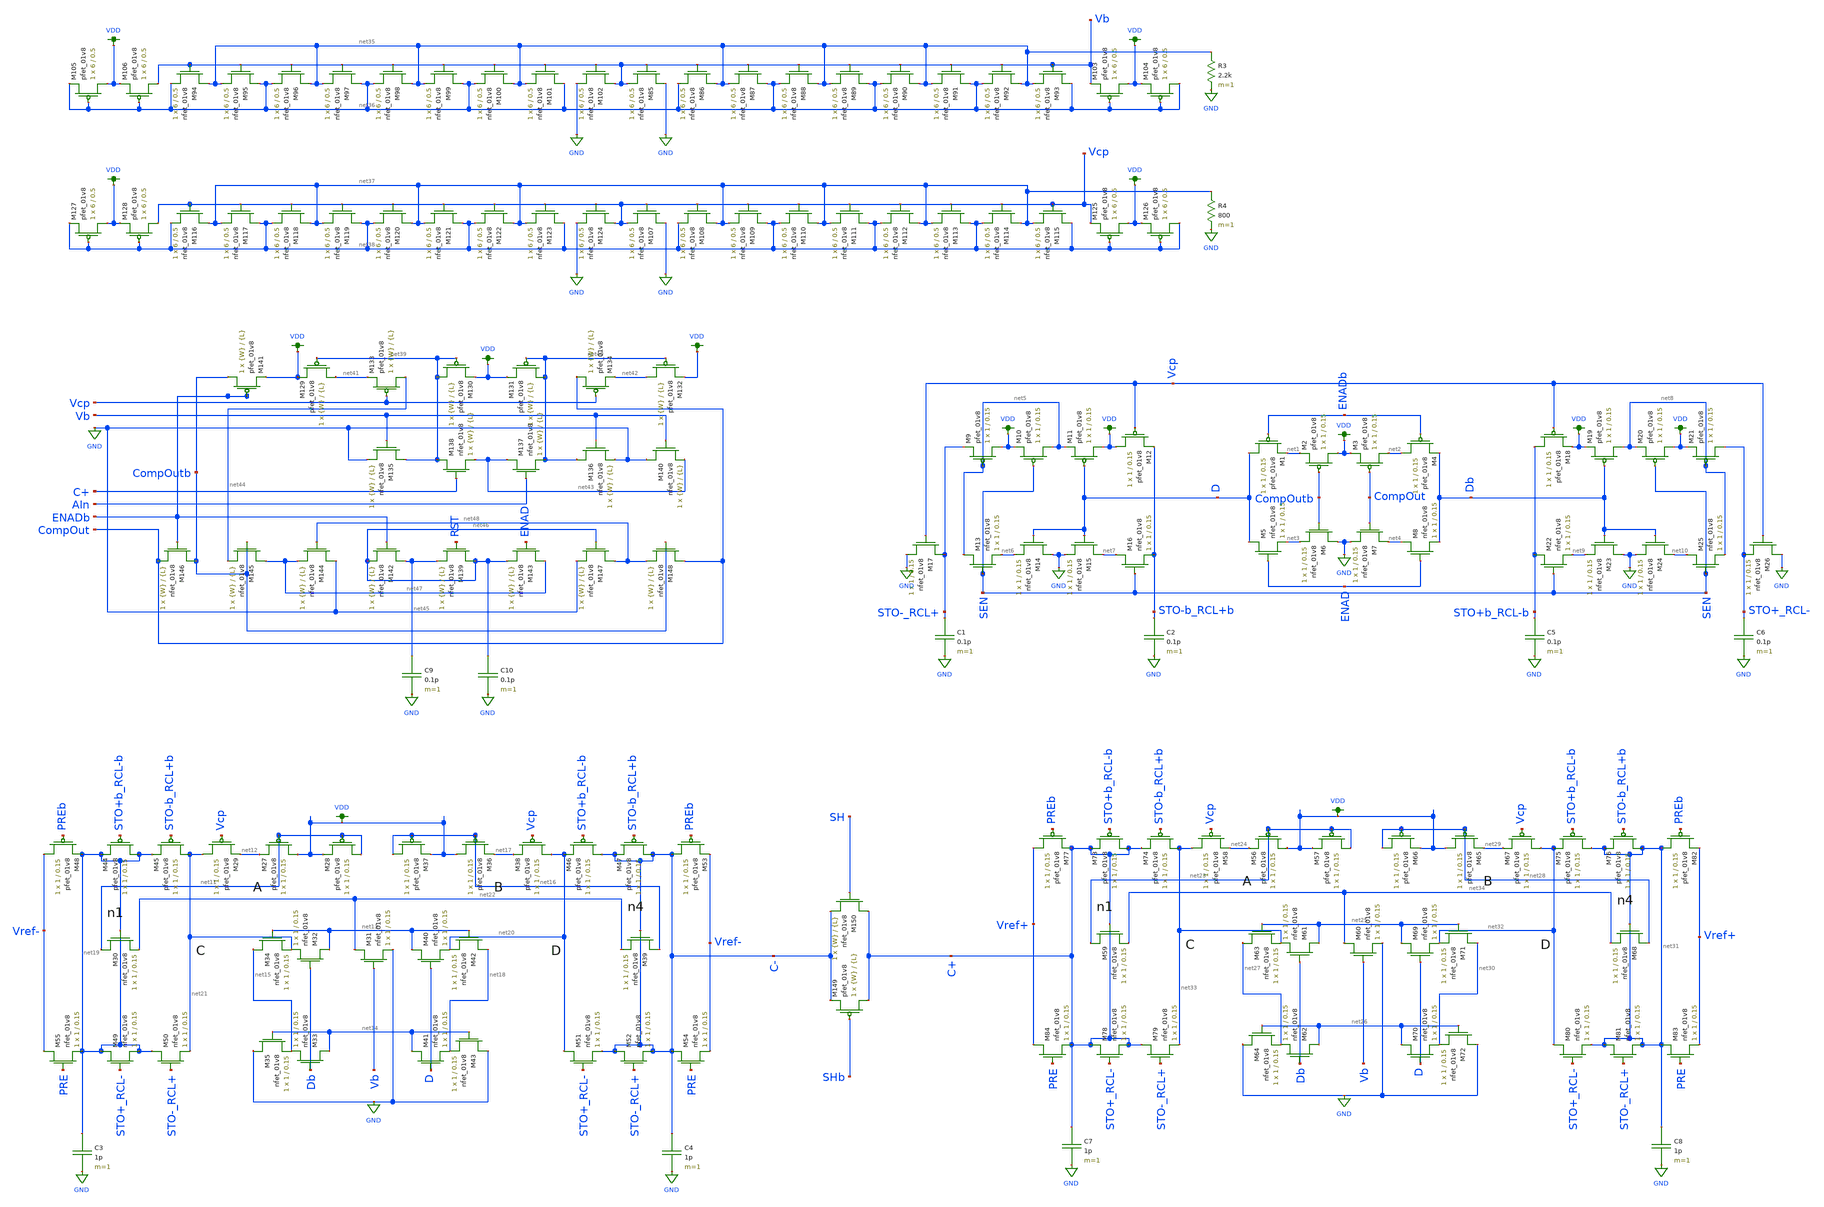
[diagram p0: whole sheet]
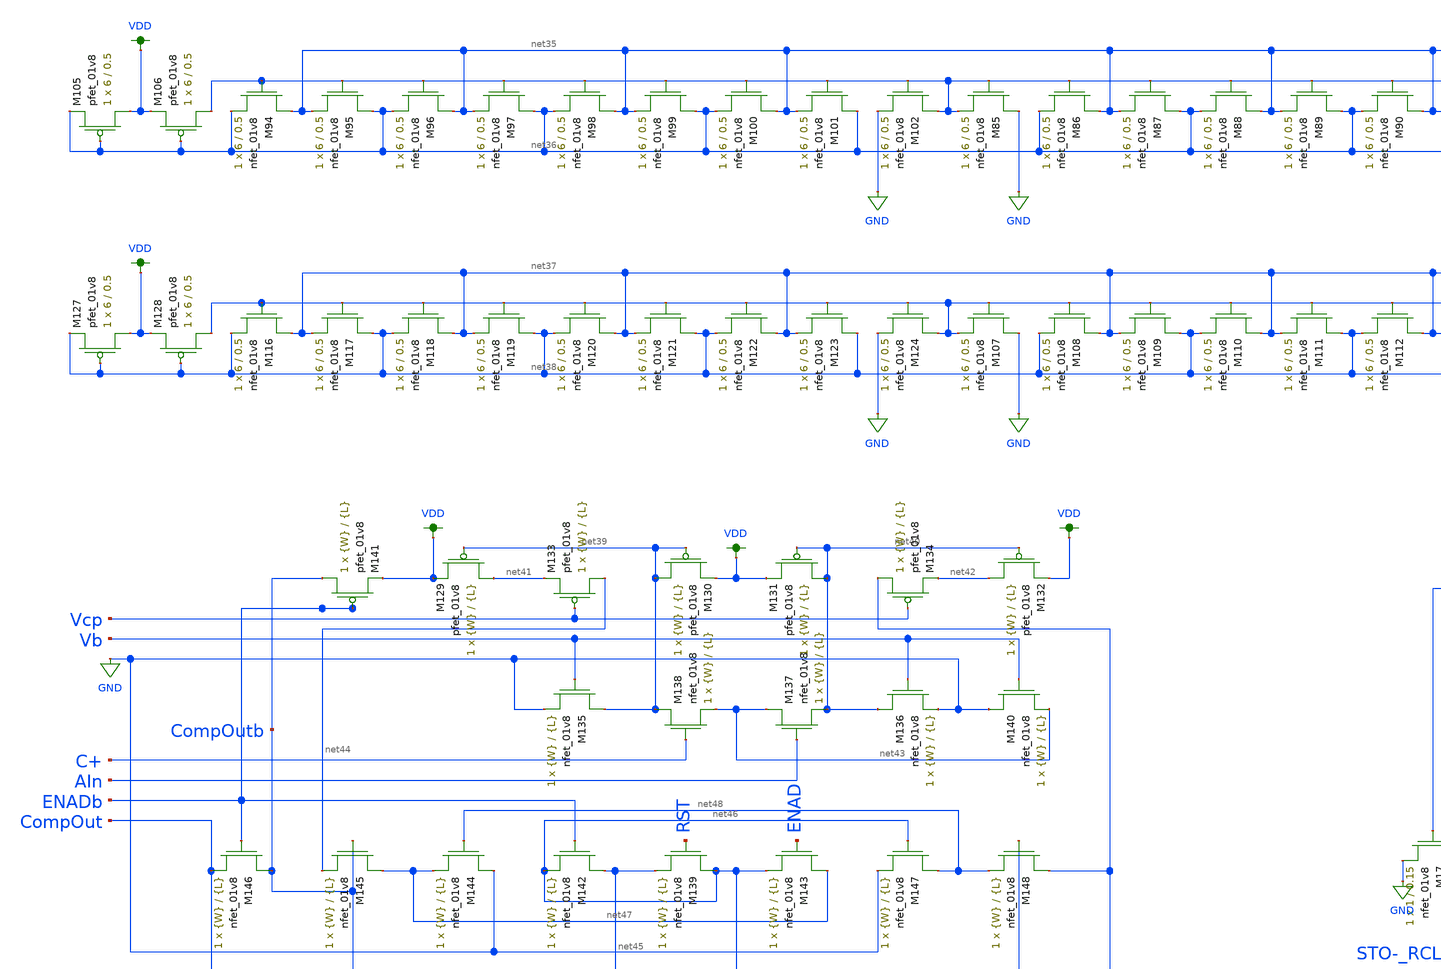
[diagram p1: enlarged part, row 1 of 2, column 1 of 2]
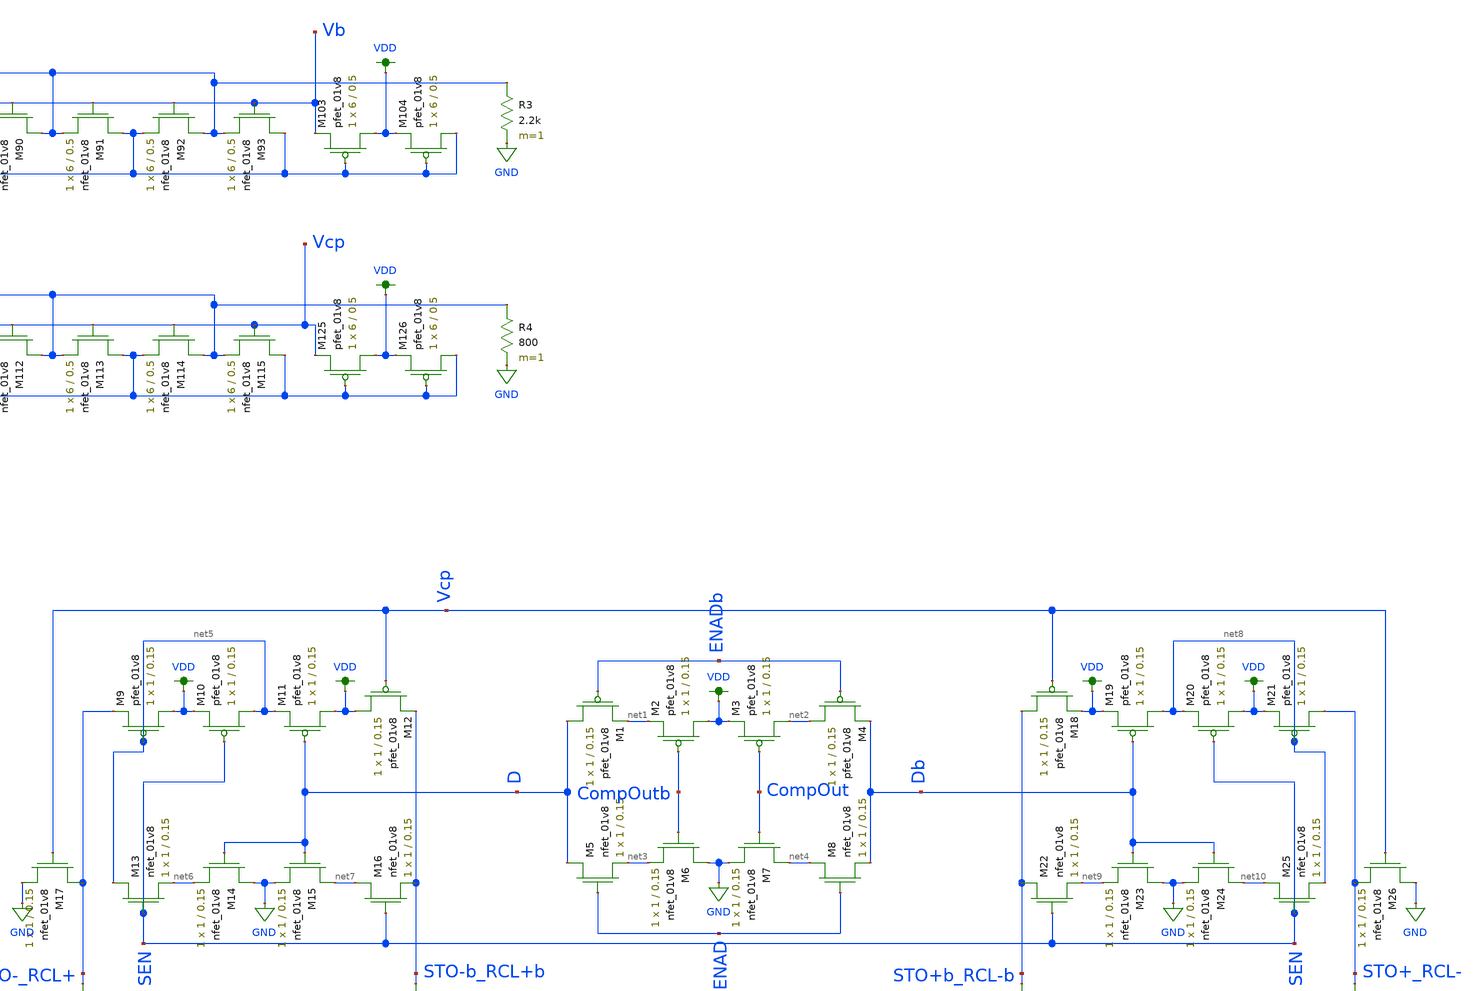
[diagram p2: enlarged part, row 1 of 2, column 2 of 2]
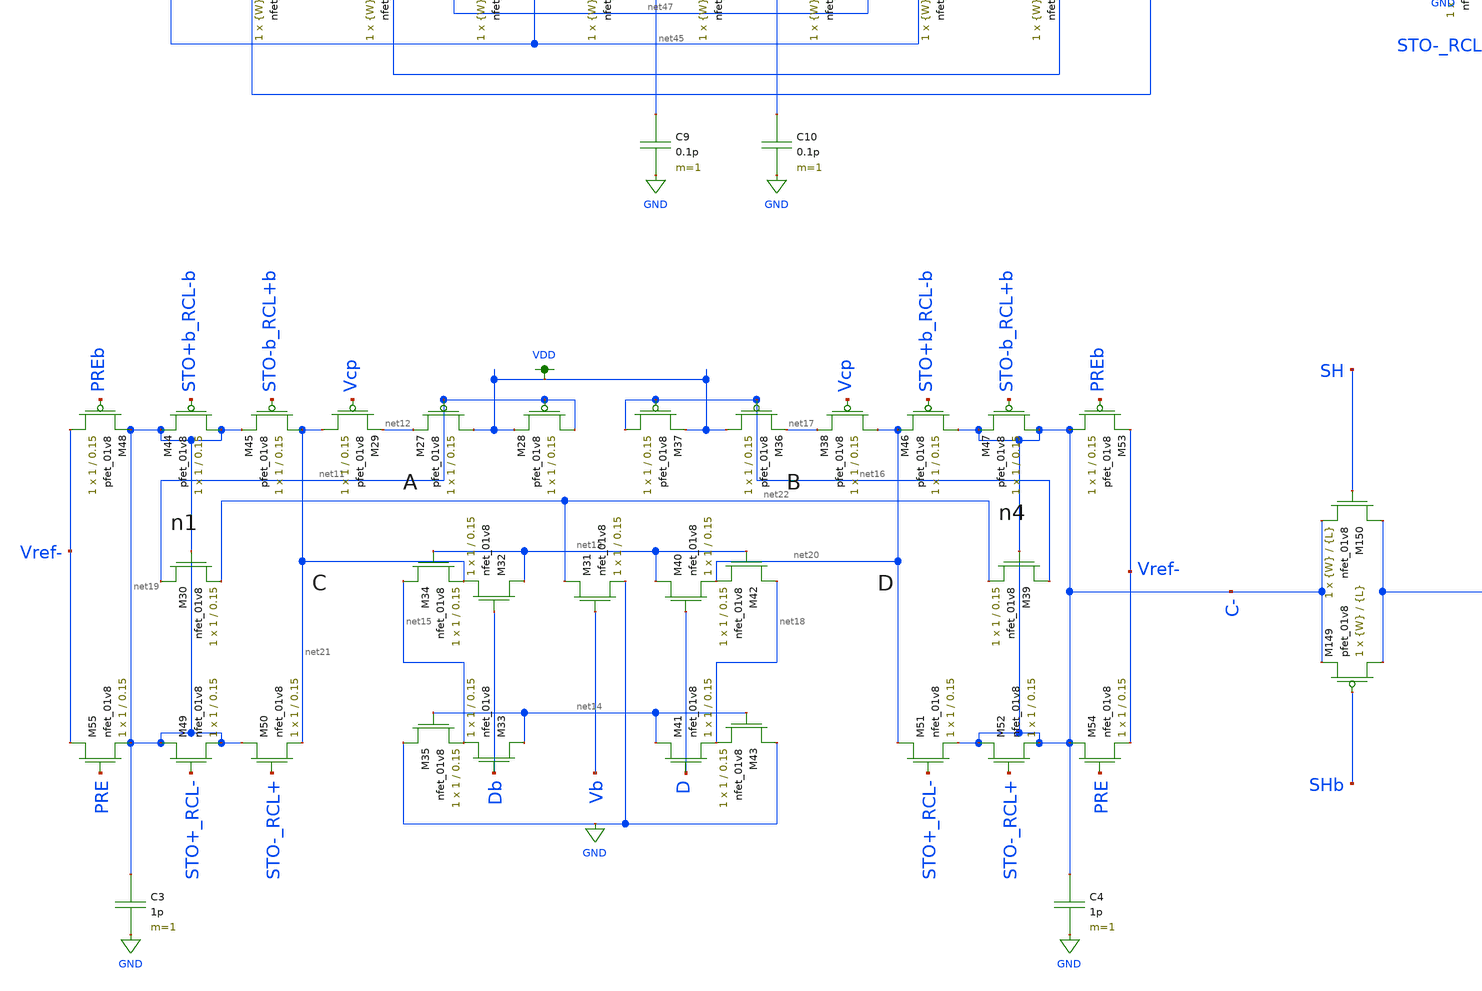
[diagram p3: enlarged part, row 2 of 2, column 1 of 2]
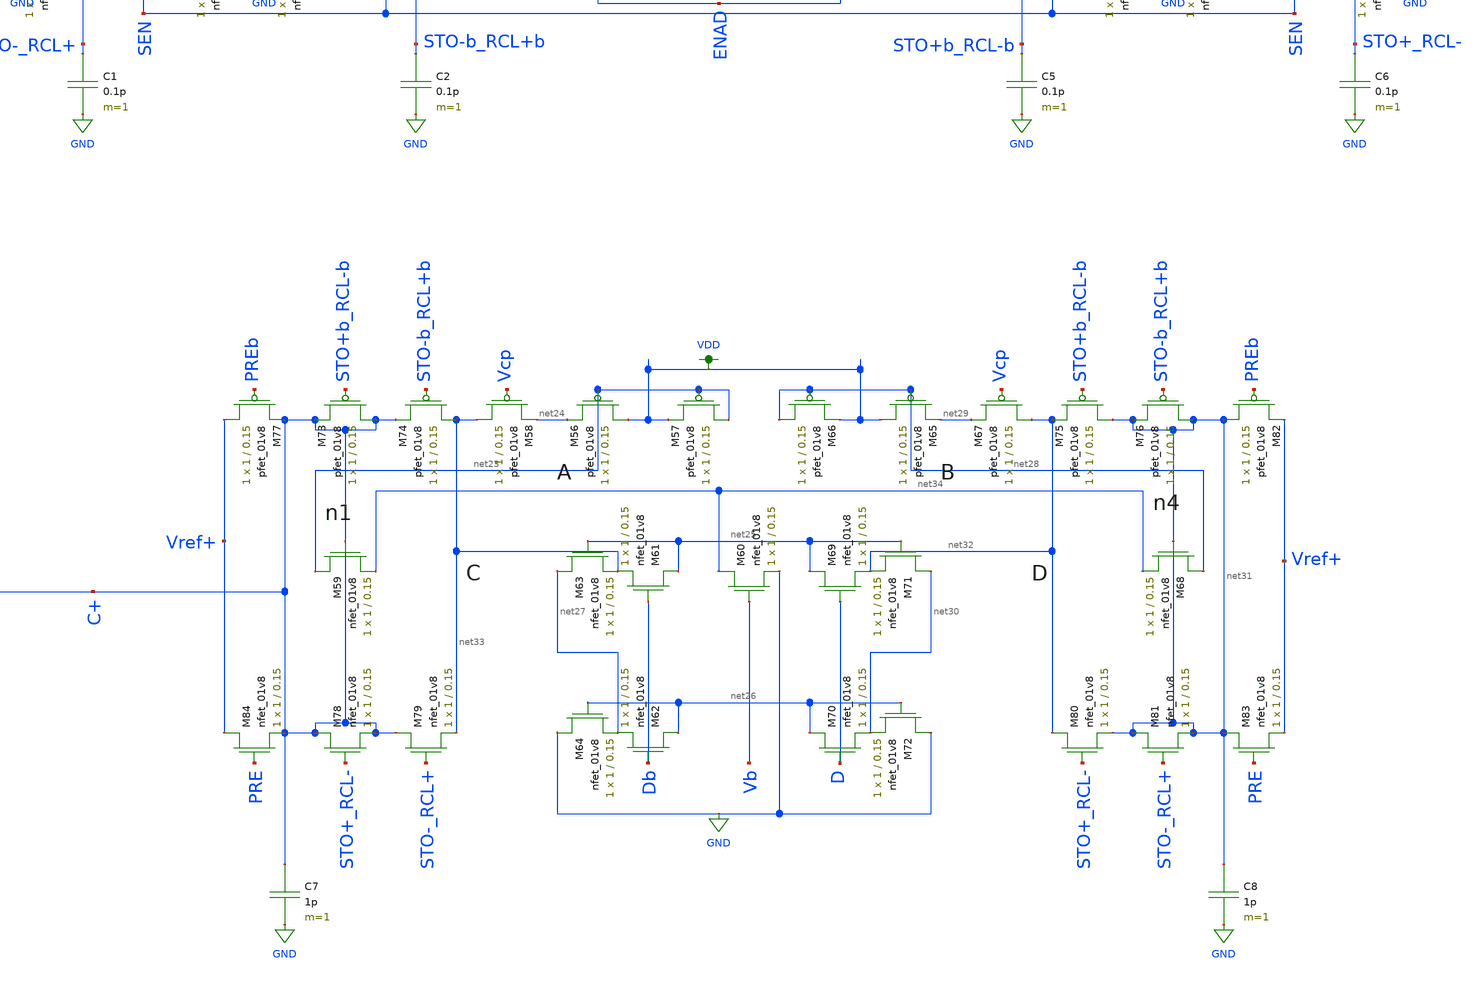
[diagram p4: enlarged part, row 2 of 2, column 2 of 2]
** sch_path: schematics/LDS/lds_schematics.sch
**.subckt lds_schematics
XM1 D ENADb net1 VDD sky130_fd_pr__pfet_01v8 L=0.15 W=1 nf=1 ad='int((nf+1)/2) * W/nf * 0.29' as='int((nf+2)/2) * W/nf * 0.29'
+ pd='2*int((nf+1)/2) * (W/nf + 0.29)' ps='2*int((nf+2)/2) * (W/nf + 0.29)' nrd='0.29 / W' nrs='0.29 / W'
+ sa=0 sb=0 sd=0 mult=1 m=1
XM2 VDD CompOutb net1 VDD sky130_fd_pr__pfet_01v8 L=0.15 W=1 nf=1 ad='int((nf+1)/2) * W/nf * 0.29' as='int((nf+2)/2) * W/nf * 0.29'
+ pd='2*int((nf+1)/2) * (W/nf + 0.29)' ps='2*int((nf+2)/2) * (W/nf + 0.29)' nrd='0.29 / W' nrs='0.29 / W'
+ sa=0 sb=0 sd=0 mult=1 m=1
XM3 net2 CompOut VDD VDD sky130_fd_pr__pfet_01v8 L=0.15 W=1 nf=1 ad='int((nf+1)/2) * W/nf * 0.29' as='int((nf+2)/2) * W/nf * 0.29'
+ pd='2*int((nf+1)/2) * (W/nf + 0.29)' ps='2*int((nf+2)/2) * (W/nf + 0.29)' nrd='0.29 / W' nrs='0.29 / W'
+ sa=0 sb=0 sd=0 mult=1 m=1
XM4 net2 ENADb Db VDD sky130_fd_pr__pfet_01v8 L=0.15 W=1 nf=1 ad='int((nf+1)/2) * W/nf * 0.29' as='int((nf+2)/2) * W/nf * 0.29'
+ pd='2*int((nf+1)/2) * (W/nf + 0.29)' ps='2*int((nf+2)/2) * (W/nf + 0.29)' nrd='0.29 / W' nrs='0.29 / W'
+ sa=0 sb=0 sd=0 mult=1 m=1
XM5 D ENAD net3 GND sky130_fd_pr__nfet_01v8 L=0.15 W=1 nf=1 ad='int((nf+1)/2) * W/nf * 0.29' as='int((nf+2)/2) * W/nf * 0.29'
+ pd='2*int((nf+1)/2) * (W/nf + 0.29)' ps='2*int((nf+2)/2) * (W/nf + 0.29)' nrd='0.29 / W' nrs='0.29 / W'
+ sa=0 sb=0 sd=0 mult=1 m=1
XM6 GND CompOutb net3 GND sky130_fd_pr__nfet_01v8 L=0.15 W=1 nf=1 ad='int((nf+1)/2) * W/nf * 0.29' as='int((nf+2)/2) * W/nf * 0.29'
+ pd='2*int((nf+1)/2) * (W/nf + 0.29)' ps='2*int((nf+2)/2) * (W/nf + 0.29)' nrd='0.29 / W' nrs='0.29 / W'
+ sa=0 sb=0 sd=0 mult=1 m=1
XM7 net4 CompOut GND GND sky130_fd_pr__nfet_01v8 L=0.15 W=1 nf=1 ad='int((nf+1)/2) * W/nf * 0.29' as='int((nf+2)/2) * W/nf * 0.29'
+ pd='2*int((nf+1)/2) * (W/nf + 0.29)' ps='2*int((nf+2)/2) * (W/nf + 0.29)' nrd='0.29 / W' nrs='0.29 / W'
+ sa=0 sb=0 sd=0 mult=1 m=1
XM8 net4 ENAD Db GND sky130_fd_pr__nfet_01v8 L=0.15 W=1 nf=1 ad='int((nf+1)/2) * W/nf * 0.29' as='int((nf+2)/2) * W/nf * 0.29'
+ pd='2*int((nf+1)/2) * (W/nf + 0.29)' ps='2*int((nf+2)/2) * (W/nf + 0.29)' nrd='0.29 / W' nrs='0.29 / W'
+ sa=0 sb=0 sd=0 mult=1 m=1
XM9 VDD net5 STO-_RCL+ VDD sky130_fd_pr__pfet_01v8 L=0.15 W=1 nf=1 ad='int((nf+1)/2) * W/nf * 0.29' as='int((nf+2)/2) * W/nf * 0.29'
+ pd='2*int((nf+1)/2) * (W/nf + 0.29)' ps='2*int((nf+2)/2) * (W/nf + 0.29)' nrd='0.29 / W' nrs='0.29 / W'
+ sa=0 sb=0 sd=0 mult=1 m=1
XM10 net5 SEN VDD VDD sky130_fd_pr__pfet_01v8 L=0.15 W=1 nf=1 ad='int((nf+1)/2) * W/nf * 0.29' as='int((nf+2)/2) * W/nf * 0.29'
+ pd='2*int((nf+1)/2) * (W/nf + 0.29)' ps='2*int((nf+2)/2) * (W/nf + 0.29)' nrd='0.29 / W' nrs='0.29 / W'
+ sa=0 sb=0 sd=0 mult=1 m=1
XM11 VDD D net5 VDD sky130_fd_pr__pfet_01v8 L=0.15 W=1 nf=1 ad='int((nf+1)/2) * W/nf * 0.29' as='int((nf+2)/2) * W/nf * 0.29'
+ pd='2*int((nf+1)/2) * (W/nf + 0.29)' ps='2*int((nf+2)/2) * (W/nf + 0.29)' nrd='0.29 / W' nrs='0.29 / W'
+ sa=0 sb=0 sd=0 mult=1 m=1
XM12 VDD Vcp STO-b_RCL+b VDD sky130_fd_pr__pfet_01v8 L=0.15 W=1 nf=1 ad='int((nf+1)/2) * W/nf * 0.29'
+ as='int((nf+2)/2) * W/nf * 0.29' pd='2*int((nf+1)/2) * (W/nf + 0.29)' ps='2*int((nf+2)/2) * (W/nf + 0.29)'
+ nrd='0.29 / W' nrs='0.29 / W' sa=0 sb=0 sd=0 mult=1 m=1
XM13 net5 SEN net6 GND sky130_fd_pr__nfet_01v8 L=0.15 W=1 nf=1 ad='int((nf+1)/2) * W/nf * 0.29' as='int((nf+2)/2) * W/nf * 0.29'
+ pd='2*int((nf+1)/2) * (W/nf + 0.29)' ps='2*int((nf+2)/2) * (W/nf + 0.29)' nrd='0.29 / W' nrs='0.29 / W'
+ sa=0 sb=0 sd=0 mult=1 m=1
XM14 GND D net6 GND sky130_fd_pr__nfet_01v8 L=0.15 W=1 nf=1 ad='int((nf+1)/2) * W/nf * 0.29' as='int((nf+2)/2) * W/nf * 0.29'
+ pd='2*int((nf+1)/2) * (W/nf + 0.29)' ps='2*int((nf+2)/2) * (W/nf + 0.29)' nrd='0.29 / W' nrs='0.29 / W'
+ sa=0 sb=0 sd=0 mult=1 m=1
XM15 net7 D GND GND sky130_fd_pr__nfet_01v8 L=0.15 W=1 nf=1 ad='int((nf+1)/2) * W/nf * 0.29' as='int((nf+2)/2) * W/nf * 0.29'
+ pd='2*int((nf+1)/2) * (W/nf + 0.29)' ps='2*int((nf+2)/2) * (W/nf + 0.29)' nrd='0.29 / W' nrs='0.29 / W'
+ sa=0 sb=0 sd=0 mult=1 m=1
XM16 net7 SEN STO-b_RCL+b GND sky130_fd_pr__nfet_01v8 L=0.15 W=1 nf=1 ad='int((nf+1)/2) * W/nf * 0.29'
+ as='int((nf+2)/2) * W/nf * 0.29' pd='2*int((nf+1)/2) * (W/nf + 0.29)' ps='2*int((nf+2)/2) * (W/nf + 0.29)'
+ nrd='0.29 / W' nrs='0.29 / W' sa=0 sb=0 sd=0 mult=1 m=1
XM17 STO-_RCL+ Vcp GND GND sky130_fd_pr__nfet_01v8 L=0.15 W=1 nf=1 ad='int((nf+1)/2) * W/nf * 0.29' as='int((nf+2)/2) * W/nf * 0.29'
+ pd='2*int((nf+1)/2) * (W/nf + 0.29)' ps='2*int((nf+2)/2) * (W/nf + 0.29)' nrd='0.29 / W' nrs='0.29 / W'
+ sa=0 sb=0 sd=0 mult=1 m=1
C1 STO-_RCL+ GND 0.1p m=1
C2 STO-b_RCL+b GND 0.1p m=1
XM18 STO+b_RCL-b Vcp VDD VDD sky130_fd_pr__pfet_01v8 L=0.15 W=1 nf=1 ad='int((nf+1)/2) * W/nf * 0.29'
+ as='int((nf+2)/2) * W/nf * 0.29' pd='2*int((nf+1)/2) * (W/nf + 0.29)' ps='2*int((nf+2)/2) * (W/nf + 0.29)'
+ nrd='0.29 / W' nrs='0.29 / W' sa=0 sb=0 sd=0 mult=1 m=1
XM19 net8 Db VDD VDD sky130_fd_pr__pfet_01v8 L=0.15 W=1 nf=1 ad='int((nf+1)/2) * W/nf * 0.29' as='int((nf+2)/2) * W/nf * 0.29'
+ pd='2*int((nf+1)/2) * (W/nf + 0.29)' ps='2*int((nf+2)/2) * (W/nf + 0.29)' nrd='0.29 / W' nrs='0.29 / W'
+ sa=0 sb=0 sd=0 mult=1 m=1
XM20 VDD SEN net8 VDD sky130_fd_pr__pfet_01v8 L=0.15 W=1 nf=1 ad='int((nf+1)/2) * W/nf * 0.29' as='int((nf+2)/2) * W/nf * 0.29'
+ pd='2*int((nf+1)/2) * (W/nf + 0.29)' ps='2*int((nf+2)/2) * (W/nf + 0.29)' nrd='0.29 / W' nrs='0.29 / W'
+ sa=0 sb=0 sd=0 mult=1 m=1
XM21 STO+_RCL- net8 VDD VDD sky130_fd_pr__pfet_01v8 L=0.15 W=1 nf=1 ad='int((nf+1)/2) * W/nf * 0.29'
+ as='int((nf+2)/2) * W/nf * 0.29' pd='2*int((nf+1)/2) * (W/nf + 0.29)' ps='2*int((nf+2)/2) * (W/nf + 0.29)'
+ nrd='0.29 / W' nrs='0.29 / W' sa=0 sb=0 sd=0 mult=1 m=1
XM22 STO+b_RCL-b SEN net9 GND sky130_fd_pr__nfet_01v8 L=0.15 W=1 nf=1 ad='int((nf+1)/2) * W/nf * 0.29'
+ as='int((nf+2)/2) * W/nf * 0.29' pd='2*int((nf+1)/2) * (W/nf + 0.29)' ps='2*int((nf+2)/2) * (W/nf + 0.29)'
+ nrd='0.29 / W' nrs='0.29 / W' sa=0 sb=0 sd=0 mult=1 m=1
XM23 GND Db net9 GND sky130_fd_pr__nfet_01v8 L=0.15 W=1 nf=1 ad='int((nf+1)/2) * W/nf * 0.29' as='int((nf+2)/2) * W/nf * 0.29'
+ pd='2*int((nf+1)/2) * (W/nf + 0.29)' ps='2*int((nf+2)/2) * (W/nf + 0.29)' nrd='0.29 / W' nrs='0.29 / W'
+ sa=0 sb=0 sd=0 mult=1 m=1
XM24 net10 Db GND GND sky130_fd_pr__nfet_01v8 L=0.15 W=1 nf=1 ad='int((nf+1)/2) * W/nf * 0.29' as='int((nf+2)/2) * W/nf * 0.29'
+ pd='2*int((nf+1)/2) * (W/nf + 0.29)' ps='2*int((nf+2)/2) * (W/nf + 0.29)' nrd='0.29 / W' nrs='0.29 / W'
+ sa=0 sb=0 sd=0 mult=1 m=1
XM25 net10 SEN net8 GND sky130_fd_pr__nfet_01v8 L=0.15 W=1 nf=1 ad='int((nf+1)/2) * W/nf * 0.29' as='int((nf+2)/2) * W/nf * 0.29'
+ pd='2*int((nf+1)/2) * (W/nf + 0.29)' ps='2*int((nf+2)/2) * (W/nf + 0.29)' nrd='0.29 / W' nrs='0.29 / W'
+ sa=0 sb=0 sd=0 mult=1 m=1
XM26 GND Vcp STO+_RCL- GND sky130_fd_pr__nfet_01v8 L=0.15 W=1 nf=1 ad='int((nf+1)/2) * W/nf * 0.29' as='int((nf+2)/2) * W/nf * 0.29'
+ pd='2*int((nf+1)/2) * (W/nf + 0.29)' ps='2*int((nf+2)/2) * (W/nf + 0.29)' nrd='0.29 / W' nrs='0.29 / W'
+ sa=0 sb=0 sd=0 mult=1 m=1
C5 STO+b_RCL-b GND 0.1p m=1
C6 STO+_RCL- GND 0.1p m=1
XM27 VDD net11 net12 VDD sky130_fd_pr__pfet_01v8 L=0.15 W=1 nf=1 ad='int((nf+1)/2) * W/nf * 0.29' as='int((nf+2)/2) * W/nf * 0.29'
+ pd='2*int((nf+1)/2) * (W/nf + 0.29)' ps='2*int((nf+2)/2) * (W/nf + 0.29)' nrd='0.29 / W' nrs='0.29 / W'
+ sa=0 sb=0 sd=0 mult=1 m=1
XM28 net11 net11 VDD VDD sky130_fd_pr__pfet_01v8 L=0.15 W=1 nf=1 ad='int((nf+1)/2) * W/nf * 0.29' as='int((nf+2)/2) * W/nf * 0.29'
+ pd='2*int((nf+1)/2) * (W/nf + 0.29)' ps='2*int((nf+2)/2) * (W/nf + 0.29)' nrd='0.29 / W' nrs='0.29 / W'
+ sa=0 sb=0 sd=0 mult=1 m=1
XM29 net21 Vcp net12 VDD sky130_fd_pr__pfet_01v8 L=0.15 W=1 nf=1 ad='int((nf+1)/2) * W/nf * 0.29' as='int((nf+2)/2) * W/nf * 0.29'
+ pd='2*int((nf+1)/2) * (W/nf + 0.29)' ps='2*int((nf+2)/2) * (W/nf + 0.29)' nrd='0.29 / W' nrs='0.29 / W'
+ sa=0 sb=0 sd=0 mult=1 m=1
XM30 net11 net19 net22 GND sky130_fd_pr__nfet_01v8 L=0.15 W=1 nf=1 ad='int((nf+1)/2) * W/nf * 0.29' as='int((nf+2)/2) * W/nf * 0.29'
+ pd='2*int((nf+1)/2) * (W/nf + 0.29)' ps='2*int((nf+2)/2) * (W/nf + 0.29)' nrd='0.29 / W' nrs='0.29 / W'
+ sa=0 sb=0 sd=0 mult=1 m=1
XM31 net22 Vb GND GND sky130_fd_pr__nfet_01v8 L=0.15 W=1 nf=1 ad='int((nf+1)/2) * W/nf * 0.29' as='int((nf+2)/2) * W/nf * 0.29'
+ pd='2*int((nf+1)/2) * (W/nf + 0.29)' ps='2*int((nf+2)/2) * (W/nf + 0.29)' nrd='0.29 / W' nrs='0.29 / W'
+ sa=0 sb=0 sd=0 mult=1 m=1
XM32 net13 Db net21 GND sky130_fd_pr__nfet_01v8 L=0.15 W=1 nf=1 ad='int((nf+1)/2) * W/nf * 0.29' as='int((nf+2)/2) * W/nf * 0.29'
+ pd='2*int((nf+1)/2) * (W/nf + 0.29)' ps='2*int((nf+2)/2) * (W/nf + 0.29)' nrd='0.29 / W' nrs='0.29 / W'
+ sa=0 sb=0 sd=0 mult=1 m=1
XM33 net14 Db net15 GND sky130_fd_pr__nfet_01v8 L=0.15 W=1 nf=1 ad='int((nf+1)/2) * W/nf * 0.29' as='int((nf+2)/2) * W/nf * 0.29'
+ pd='2*int((nf+1)/2) * (W/nf + 0.29)' ps='2*int((nf+2)/2) * (W/nf + 0.29)' nrd='0.29 / W' nrs='0.29 / W'
+ sa=0 sb=0 sd=0 mult=1 m=1
XM34 net15 net13 net21 GND sky130_fd_pr__nfet_01v8 L=0.15 W=1 nf=1 ad='int((nf+1)/2) * W/nf * 0.29' as='int((nf+2)/2) * W/nf * 0.29'
+ pd='2*int((nf+1)/2) * (W/nf + 0.29)' ps='2*int((nf+2)/2) * (W/nf + 0.29)' nrd='0.29 / W' nrs='0.29 / W'
+ sa=0 sb=0 sd=0 mult=1 m=1
XM35 GND net14 net15 GND sky130_fd_pr__nfet_01v8 L=0.15 W=1 nf=1 ad='int((nf+1)/2) * W/nf * 0.29' as='int((nf+2)/2) * W/nf * 0.29'
+ pd='2*int((nf+1)/2) * (W/nf + 0.29)' ps='2*int((nf+2)/2) * (W/nf + 0.29)' nrd='0.29 / W' nrs='0.29 / W'
+ sa=0 sb=0 sd=0 mult=1 m=1
XM36 VDD net16 net17 VDD sky130_fd_pr__pfet_01v8 L=0.15 W=1 nf=1 ad='int((nf+1)/2) * W/nf * 0.29' as='int((nf+2)/2) * W/nf * 0.29'
+ pd='2*int((nf+1)/2) * (W/nf + 0.29)' ps='2*int((nf+2)/2) * (W/nf + 0.29)' nrd='0.29 / W' nrs='0.29 / W'
+ sa=0 sb=0 sd=0 mult=1 m=1
XM37 net16 net16 VDD VDD sky130_fd_pr__pfet_01v8 L=0.15 W=1 nf=1 ad='int((nf+1)/2) * W/nf * 0.29' as='int((nf+2)/2) * W/nf * 0.29'
+ pd='2*int((nf+1)/2) * (W/nf + 0.29)' ps='2*int((nf+2)/2) * (W/nf + 0.29)' nrd='0.29 / W' nrs='0.29 / W'
+ sa=0 sb=0 sd=0 mult=1 m=1
XM38 net20 Vcp net17 VDD sky130_fd_pr__pfet_01v8 L=0.15 W=1 nf=1 ad='int((nf+1)/2) * W/nf * 0.29' as='int((nf+2)/2) * W/nf * 0.29'
+ pd='2*int((nf+1)/2) * (W/nf + 0.29)' ps='2*int((nf+2)/2) * (W/nf + 0.29)' nrd='0.29 / W' nrs='0.29 / W'
+ sa=0 sb=0 sd=0 mult=1 m=1
XM39 net16 C- net22 GND sky130_fd_pr__nfet_01v8 L=0.15 W=1 nf=1 ad='int((nf+1)/2) * W/nf * 0.29' as='int((nf+2)/2) * W/nf * 0.29'
+ pd='2*int((nf+1)/2) * (W/nf + 0.29)' ps='2*int((nf+2)/2) * (W/nf + 0.29)' nrd='0.29 / W' nrs='0.29 / W'
+ sa=0 sb=0 sd=0 mult=1 m=1
XM40 net13 D net20 GND sky130_fd_pr__nfet_01v8 L=0.15 W=1 nf=1 ad='int((nf+1)/2) * W/nf * 0.29' as='int((nf+2)/2) * W/nf * 0.29'
+ pd='2*int((nf+1)/2) * (W/nf + 0.29)' ps='2*int((nf+2)/2) * (W/nf + 0.29)' nrd='0.29 / W' nrs='0.29 / W'
+ sa=0 sb=0 sd=0 mult=1 m=1
XM41 net14 D net18 GND sky130_fd_pr__nfet_01v8 L=0.15 W=1 nf=1 ad='int((nf+1)/2) * W/nf * 0.29' as='int((nf+2)/2) * W/nf * 0.29'
+ pd='2*int((nf+1)/2) * (W/nf + 0.29)' ps='2*int((nf+2)/2) * (W/nf + 0.29)' nrd='0.29 / W' nrs='0.29 / W'
+ sa=0 sb=0 sd=0 mult=1 m=1
XM42 net18 net13 net20 GND sky130_fd_pr__nfet_01v8 L=0.15 W=1 nf=1 ad='int((nf+1)/2) * W/nf * 0.29' as='int((nf+2)/2) * W/nf * 0.29'
+ pd='2*int((nf+1)/2) * (W/nf + 0.29)' ps='2*int((nf+2)/2) * (W/nf + 0.29)' nrd='0.29 / W' nrs='0.29 / W'
+ sa=0 sb=0 sd=0 mult=1 m=1
XM43 GND net14 net18 GND sky130_fd_pr__nfet_01v8 L=0.15 W=1 nf=1 ad='int((nf+1)/2) * W/nf * 0.29' as='int((nf+2)/2) * W/nf * 0.29'
+ pd='2*int((nf+1)/2) * (W/nf + 0.29)' ps='2*int((nf+2)/2) * (W/nf + 0.29)' nrd='0.29 / W' nrs='0.29 / W'
+ sa=0 sb=0 sd=0 mult=1 m=1
XM44 net19 STO+b_RCL-b net19 VDD sky130_fd_pr__pfet_01v8 L=0.15 W=1 nf=1 ad='int((nf+1)/2) * W/nf * 0.29'
+ as='int((nf+2)/2) * W/nf * 0.29' pd='2*int((nf+1)/2) * (W/nf + 0.29)' ps='2*int((nf+2)/2) * (W/nf + 0.29)'
+ nrd='0.29 / W' nrs='0.29 / W' sa=0 sb=0 sd=0 mult=1 m=1
XM45 net21 STO-b_RCL+b net19 VDD sky130_fd_pr__pfet_01v8 L=0.15 W=1 nf=1 ad='int((nf+1)/2) * W/nf * 0.29'
+ as='int((nf+2)/2) * W/nf * 0.29' pd='2*int((nf+1)/2) * (W/nf + 0.29)' ps='2*int((nf+2)/2) * (W/nf + 0.29)'
+ nrd='0.29 / W' nrs='0.29 / W' sa=0 sb=0 sd=0 mult=1 m=1
XM46 C- STO+b_RCL-b net20 VDD sky130_fd_pr__pfet_01v8 L=0.15 W=1 nf=1 ad='int((nf+1)/2) * W/nf * 0.29'
+ as='int((nf+2)/2) * W/nf * 0.29' pd='2*int((nf+1)/2) * (W/nf + 0.29)' ps='2*int((nf+2)/2) * (W/nf + 0.29)'
+ nrd='0.29 / W' nrs='0.29 / W' sa=0 sb=0 sd=0 mult=1 m=1
XM47 C- STO-b_RCL+b C- VDD sky130_fd_pr__pfet_01v8 L=0.15 W=1 nf=1 ad='int((nf+1)/2) * W/nf * 0.29' as='int((nf+2)/2) * W/nf * 0.29'
+ pd='2*int((nf+1)/2) * (W/nf + 0.29)' ps='2*int((nf+2)/2) * (W/nf + 0.29)' nrd='0.29 / W' nrs='0.29 / W'
+ sa=0 sb=0 sd=0 mult=1 m=1
XM48 Vref- PREb net19 VDD sky130_fd_pr__pfet_01v8 L=0.15 W=1 nf=1 ad='int((nf+1)/2) * W/nf * 0.29' as='int((nf+2)/2) * W/nf * 0.29'
+ pd='2*int((nf+1)/2) * (W/nf + 0.29)' ps='2*int((nf+2)/2) * (W/nf + 0.29)' nrd='0.29 / W' nrs='0.29 / W'
+ sa=0 sb=0 sd=0 mult=1 m=1
XM49 net19 STO+_RCL- net19 GND sky130_fd_pr__nfet_01v8 L=0.15 W=1 nf=1 ad='int((nf+1)/2) * W/nf * 0.29'
+ as='int((nf+2)/2) * W/nf * 0.29' pd='2*int((nf+1)/2) * (W/nf + 0.29)' ps='2*int((nf+2)/2) * (W/nf + 0.29)'
+ nrd='0.29 / W' nrs='0.29 / W' sa=0 sb=0 sd=0 mult=1 m=1
XM50 net19 STO-_RCL+ net21 GND sky130_fd_pr__nfet_01v8 L=0.15 W=1 nf=1 ad='int((nf+1)/2) * W/nf * 0.29'
+ as='int((nf+2)/2) * W/nf * 0.29' pd='2*int((nf+1)/2) * (W/nf + 0.29)' ps='2*int((nf+2)/2) * (W/nf + 0.29)'
+ nrd='0.29 / W' nrs='0.29 / W' sa=0 sb=0 sd=0 mult=1 m=1
XM51 net20 STO+_RCL- C- GND sky130_fd_pr__nfet_01v8 L=0.15 W=1 nf=1 ad='int((nf+1)/2) * W/nf * 0.29'
+ as='int((nf+2)/2) * W/nf * 0.29' pd='2*int((nf+1)/2) * (W/nf + 0.29)' ps='2*int((nf+2)/2) * (W/nf + 0.29)'
+ nrd='0.29 / W' nrs='0.29 / W' sa=0 sb=0 sd=0 mult=1 m=1
XM52 C- STO-_RCL+ C- GND sky130_fd_pr__nfet_01v8 L=0.15 W=1 nf=1 ad='int((nf+1)/2) * W/nf * 0.29' as='int((nf+2)/2) * W/nf * 0.29'
+ pd='2*int((nf+1)/2) * (W/nf + 0.29)' ps='2*int((nf+2)/2) * (W/nf + 0.29)' nrd='0.29 / W' nrs='0.29 / W'
+ sa=0 sb=0 sd=0 mult=1 m=1
XM53 C- PREb Vref- VDD sky130_fd_pr__pfet_01v8 L=0.15 W=1 nf=1 ad='int((nf+1)/2) * W/nf * 0.29' as='int((nf+2)/2) * W/nf * 0.29'
+ pd='2*int((nf+1)/2) * (W/nf + 0.29)' ps='2*int((nf+2)/2) * (W/nf + 0.29)' nrd='0.29 / W' nrs='0.29 / W'
+ sa=0 sb=0 sd=0 mult=1 m=1
XM54 C- PRE Vref- GND sky130_fd_pr__nfet_01v8 L=0.15 W=1 nf=1 ad='int((nf+1)/2) * W/nf * 0.29' as='int((nf+2)/2) * W/nf * 0.29'
+ pd='2*int((nf+1)/2) * (W/nf + 0.29)' ps='2*int((nf+2)/2) * (W/nf + 0.29)' nrd='0.29 / W' nrs='0.29 / W'
+ sa=0 sb=0 sd=0 mult=1 m=1
XM55 Vref- PRE net19 GND sky130_fd_pr__nfet_01v8 L=0.15 W=1 nf=1 ad='int((nf+1)/2) * W/nf * 0.29' as='int((nf+2)/2) * W/nf * 0.29'
+ pd='2*int((nf+1)/2) * (W/nf + 0.29)' ps='2*int((nf+2)/2) * (W/nf + 0.29)' nrd='0.29 / W' nrs='0.29 / W'
+ sa=0 sb=0 sd=0 mult=1 m=1
C3 net19 GND 1p m=1
C4 C- GND 1p m=1
XM56 VDD net23 net24 VDD sky130_fd_pr__pfet_01v8 L=0.15 W=1 nf=1 ad='int((nf+1)/2) * W/nf * 0.29' as='int((nf+2)/2) * W/nf * 0.29'
+ pd='2*int((nf+1)/2) * (W/nf + 0.29)' ps='2*int((nf+2)/2) * (W/nf + 0.29)' nrd='0.29 / W' nrs='0.29 / W'
+ sa=0 sb=0 sd=0 mult=1 m=1
XM57 net23 net23 VDD VDD sky130_fd_pr__pfet_01v8 L=0.15 W=1 nf=1 ad='int((nf+1)/2) * W/nf * 0.29' as='int((nf+2)/2) * W/nf * 0.29'
+ pd='2*int((nf+1)/2) * (W/nf + 0.29)' ps='2*int((nf+2)/2) * (W/nf + 0.29)' nrd='0.29 / W' nrs='0.29 / W'
+ sa=0 sb=0 sd=0 mult=1 m=1
XM58 net33 Vcp net24 VDD sky130_fd_pr__pfet_01v8 L=0.15 W=1 nf=1 ad='int((nf+1)/2) * W/nf * 0.29' as='int((nf+2)/2) * W/nf * 0.29'
+ pd='2*int((nf+1)/2) * (W/nf + 0.29)' ps='2*int((nf+2)/2) * (W/nf + 0.29)' nrd='0.29 / W' nrs='0.29 / W'
+ sa=0 sb=0 sd=0 mult=1 m=1
XM59 net23 C+ net34 GND sky130_fd_pr__nfet_01v8 L=0.15 W=1 nf=1 ad='int((nf+1)/2) * W/nf * 0.29' as='int((nf+2)/2) * W/nf * 0.29'
+ pd='2*int((nf+1)/2) * (W/nf + 0.29)' ps='2*int((nf+2)/2) * (W/nf + 0.29)' nrd='0.29 / W' nrs='0.29 / W'
+ sa=0 sb=0 sd=0 mult=1 m=1
XM60 net34 Vb GND GND sky130_fd_pr__nfet_01v8 L=0.15 W=1 nf=1 ad='int((nf+1)/2) * W/nf * 0.29' as='int((nf+2)/2) * W/nf * 0.29'
+ pd='2*int((nf+1)/2) * (W/nf + 0.29)' ps='2*int((nf+2)/2) * (W/nf + 0.29)' nrd='0.29 / W' nrs='0.29 / W'
+ sa=0 sb=0 sd=0 mult=1 m=1
XM61 net25 Db net33 GND sky130_fd_pr__nfet_01v8 L=0.15 W=1 nf=1 ad='int((nf+1)/2) * W/nf * 0.29' as='int((nf+2)/2) * W/nf * 0.29'
+ pd='2*int((nf+1)/2) * (W/nf + 0.29)' ps='2*int((nf+2)/2) * (W/nf + 0.29)' nrd='0.29 / W' nrs='0.29 / W'
+ sa=0 sb=0 sd=0 mult=1 m=1
XM62 net26 Db net27 GND sky130_fd_pr__nfet_01v8 L=0.15 W=1 nf=1 ad='int((nf+1)/2) * W/nf * 0.29' as='int((nf+2)/2) * W/nf * 0.29'
+ pd='2*int((nf+1)/2) * (W/nf + 0.29)' ps='2*int((nf+2)/2) * (W/nf + 0.29)' nrd='0.29 / W' nrs='0.29 / W'
+ sa=0 sb=0 sd=0 mult=1 m=1
XM63 net27 net25 net33 GND sky130_fd_pr__nfet_01v8 L=0.15 W=1 nf=1 ad='int((nf+1)/2) * W/nf * 0.29' as='int((nf+2)/2) * W/nf * 0.29'
+ pd='2*int((nf+1)/2) * (W/nf + 0.29)' ps='2*int((nf+2)/2) * (W/nf + 0.29)' nrd='0.29 / W' nrs='0.29 / W'
+ sa=0 sb=0 sd=0 mult=1 m=1
XM64 GND net26 net27 GND sky130_fd_pr__nfet_01v8 L=0.15 W=1 nf=1 ad='int((nf+1)/2) * W/nf * 0.29' as='int((nf+2)/2) * W/nf * 0.29'
+ pd='2*int((nf+1)/2) * (W/nf + 0.29)' ps='2*int((nf+2)/2) * (W/nf + 0.29)' nrd='0.29 / W' nrs='0.29 / W'
+ sa=0 sb=0 sd=0 mult=1 m=1
XM65 VDD net28 net29 VDD sky130_fd_pr__pfet_01v8 L=0.15 W=1 nf=1 ad='int((nf+1)/2) * W/nf * 0.29' as='int((nf+2)/2) * W/nf * 0.29'
+ pd='2*int((nf+1)/2) * (W/nf + 0.29)' ps='2*int((nf+2)/2) * (W/nf + 0.29)' nrd='0.29 / W' nrs='0.29 / W'
+ sa=0 sb=0 sd=0 mult=1 m=1
XM66 net28 net28 VDD VDD sky130_fd_pr__pfet_01v8 L=0.15 W=1 nf=1 ad='int((nf+1)/2) * W/nf * 0.29' as='int((nf+2)/2) * W/nf * 0.29'
+ pd='2*int((nf+1)/2) * (W/nf + 0.29)' ps='2*int((nf+2)/2) * (W/nf + 0.29)' nrd='0.29 / W' nrs='0.29 / W'
+ sa=0 sb=0 sd=0 mult=1 m=1
XM67 net32 Vcp net29 VDD sky130_fd_pr__pfet_01v8 L=0.15 W=1 nf=1 ad='int((nf+1)/2) * W/nf * 0.29' as='int((nf+2)/2) * W/nf * 0.29'
+ pd='2*int((nf+1)/2) * (W/nf + 0.29)' ps='2*int((nf+2)/2) * (W/nf + 0.29)' nrd='0.29 / W' nrs='0.29 / W'
+ sa=0 sb=0 sd=0 mult=1 m=1
XM68 net28 net31 net34 GND sky130_fd_pr__nfet_01v8 L=0.15 W=1 nf=1 ad='int((nf+1)/2) * W/nf * 0.29' as='int((nf+2)/2) * W/nf * 0.29'
+ pd='2*int((nf+1)/2) * (W/nf + 0.29)' ps='2*int((nf+2)/2) * (W/nf + 0.29)' nrd='0.29 / W' nrs='0.29 / W'
+ sa=0 sb=0 sd=0 mult=1 m=1
XM69 net25 D net32 GND sky130_fd_pr__nfet_01v8 L=0.15 W=1 nf=1 ad='int((nf+1)/2) * W/nf * 0.29' as='int((nf+2)/2) * W/nf * 0.29'
+ pd='2*int((nf+1)/2) * (W/nf + 0.29)' ps='2*int((nf+2)/2) * (W/nf + 0.29)' nrd='0.29 / W' nrs='0.29 / W'
+ sa=0 sb=0 sd=0 mult=1 m=1
XM70 net26 D net30 GND sky130_fd_pr__nfet_01v8 L=0.15 W=1 nf=1 ad='int((nf+1)/2) * W/nf * 0.29' as='int((nf+2)/2) * W/nf * 0.29'
+ pd='2*int((nf+1)/2) * (W/nf + 0.29)' ps='2*int((nf+2)/2) * (W/nf + 0.29)' nrd='0.29 / W' nrs='0.29 / W'
+ sa=0 sb=0 sd=0 mult=1 m=1
XM71 net30 net25 net32 GND sky130_fd_pr__nfet_01v8 L=0.15 W=1 nf=1 ad='int((nf+1)/2) * W/nf * 0.29' as='int((nf+2)/2) * W/nf * 0.29'
+ pd='2*int((nf+1)/2) * (W/nf + 0.29)' ps='2*int((nf+2)/2) * (W/nf + 0.29)' nrd='0.29 / W' nrs='0.29 / W'
+ sa=0 sb=0 sd=0 mult=1 m=1
XM72 GND net26 net30 GND sky130_fd_pr__nfet_01v8 L=0.15 W=1 nf=1 ad='int((nf+1)/2) * W/nf * 0.29' as='int((nf+2)/2) * W/nf * 0.29'
+ pd='2*int((nf+1)/2) * (W/nf + 0.29)' ps='2*int((nf+2)/2) * (W/nf + 0.29)' nrd='0.29 / W' nrs='0.29 / W'
+ sa=0 sb=0 sd=0 mult=1 m=1
XM73 C+ STO+b_RCL-b C+ VDD sky130_fd_pr__pfet_01v8 L=0.15 W=1 nf=1 ad='int((nf+1)/2) * W/nf * 0.29' as='int((nf+2)/2) * W/nf * 0.29'
+ pd='2*int((nf+1)/2) * (W/nf + 0.29)' ps='2*int((nf+2)/2) * (W/nf + 0.29)' nrd='0.29 / W' nrs='0.29 / W'
+ sa=0 sb=0 sd=0 mult=1 m=1
XM74 net33 STO-b_RCL+b C+ VDD sky130_fd_pr__pfet_01v8 L=0.15 W=1 nf=1 ad='int((nf+1)/2) * W/nf * 0.29'
+ as='int((nf+2)/2) * W/nf * 0.29' pd='2*int((nf+1)/2) * (W/nf + 0.29)' ps='2*int((nf+2)/2) * (W/nf + 0.29)'
+ nrd='0.29 / W' nrs='0.29 / W' sa=0 sb=0 sd=0 mult=1 m=1
XM75 net31 STO+b_RCL-b net32 VDD sky130_fd_pr__pfet_01v8 L=0.15 W=1 nf=1 ad='int((nf+1)/2) * W/nf * 0.29'
+ as='int((nf+2)/2) * W/nf * 0.29' pd='2*int((nf+1)/2) * (W/nf + 0.29)' ps='2*int((nf+2)/2) * (W/nf + 0.29)'
+ nrd='0.29 / W' nrs='0.29 / W' sa=0 sb=0 sd=0 mult=1 m=1
XM76 net31 STO-b_RCL+b net31 VDD sky130_fd_pr__pfet_01v8 L=0.15 W=1 nf=1 ad='int((nf+1)/2) * W/nf * 0.29'
+ as='int((nf+2)/2) * W/nf * 0.29' pd='2*int((nf+1)/2) * (W/nf + 0.29)' ps='2*int((nf+2)/2) * (W/nf + 0.29)'
+ nrd='0.29 / W' nrs='0.29 / W' sa=0 sb=0 sd=0 mult=1 m=1
XM77 Vref+ PREb C+ VDD sky130_fd_pr__pfet_01v8 L=0.15 W=1 nf=1 ad='int((nf+1)/2) * W/nf * 0.29' as='int((nf+2)/2) * W/nf * 0.29'
+ pd='2*int((nf+1)/2) * (W/nf + 0.29)' ps='2*int((nf+2)/2) * (W/nf + 0.29)' nrd='0.29 / W' nrs='0.29 / W'
+ sa=0 sb=0 sd=0 mult=1 m=1
XM78 C+ STO+_RCL- C+ GND sky130_fd_pr__nfet_01v8 L=0.15 W=1 nf=1 ad='int((nf+1)/2) * W/nf * 0.29' as='int((nf+2)/2) * W/nf * 0.29'
+ pd='2*int((nf+1)/2) * (W/nf + 0.29)' ps='2*int((nf+2)/2) * (W/nf + 0.29)' nrd='0.29 / W' nrs='0.29 / W'
+ sa=0 sb=0 sd=0 mult=1 m=1
XM79 C+ STO-_RCL+ net33 GND sky130_fd_pr__nfet_01v8 L=0.15 W=1 nf=1 ad='int((nf+1)/2) * W/nf * 0.29'
+ as='int((nf+2)/2) * W/nf * 0.29' pd='2*int((nf+1)/2) * (W/nf + 0.29)' ps='2*int((nf+2)/2) * (W/nf + 0.29)'
+ nrd='0.29 / W' nrs='0.29 / W' sa=0 sb=0 sd=0 mult=1 m=1
XM80 net32 STO+_RCL- net31 GND sky130_fd_pr__nfet_01v8 L=0.15 W=1 nf=1 ad='int((nf+1)/2) * W/nf * 0.29'
+ as='int((nf+2)/2) * W/nf * 0.29' pd='2*int((nf+1)/2) * (W/nf + 0.29)' ps='2*int((nf+2)/2) * (W/nf + 0.29)'
+ nrd='0.29 / W' nrs='0.29 / W' sa=0 sb=0 sd=0 mult=1 m=1
XM81 net31 STO-_RCL+ net31 GND sky130_fd_pr__nfet_01v8 L=0.15 W=1 nf=1 ad='int((nf+1)/2) * W/nf * 0.29'
+ as='int((nf+2)/2) * W/nf * 0.29' pd='2*int((nf+1)/2) * (W/nf + 0.29)' ps='2*int((nf+2)/2) * (W/nf + 0.29)'
+ nrd='0.29 / W' nrs='0.29 / W' sa=0 sb=0 sd=0 mult=1 m=1
XM82 net31 PREb Vref+ VDD sky130_fd_pr__pfet_01v8 L=0.15 W=1 nf=1 ad='int((nf+1)/2) * W/nf * 0.29' as='int((nf+2)/2) * W/nf * 0.29'
+ pd='2*int((nf+1)/2) * (W/nf + 0.29)' ps='2*int((nf+2)/2) * (W/nf + 0.29)' nrd='0.29 / W' nrs='0.29 / W'
+ sa=0 sb=0 sd=0 mult=1 m=1
XM83 net31 PRE Vref+ GND sky130_fd_pr__nfet_01v8 L=0.15 W=1 nf=1 ad='int((nf+1)/2) * W/nf * 0.29' as='int((nf+2)/2) * W/nf * 0.29'
+ pd='2*int((nf+1)/2) * (W/nf + 0.29)' ps='2*int((nf+2)/2) * (W/nf + 0.29)' nrd='0.29 / W' nrs='0.29 / W'
+ sa=0 sb=0 sd=0 mult=1 m=1
XM84 Vref+ PRE C+ GND sky130_fd_pr__nfet_01v8 L=0.15 W=1 nf=1 ad='int((nf+1)/2) * W/nf * 0.29' as='int((nf+2)/2) * W/nf * 0.29'
+ pd='2*int((nf+1)/2) * (W/nf + 0.29)' ps='2*int((nf+2)/2) * (W/nf + 0.29)' nrd='0.29 / W' nrs='0.29 / W'
+ sa=0 sb=0 sd=0 mult=1 m=1
C7 C+ GND 1p m=1
C8 net31 GND 1p m=1
XM85 GND Vb Vb GND sky130_fd_pr__nfet_01v8 L=0.5 W=6 nf=1 ad='int((nf+1)/2) * W/nf * 0.29' as='int((nf+2)/2) * W/nf * 0.29'
+ pd='2*int((nf+1)/2) * (W/nf + 0.29)' ps='2*int((nf+2)/2) * (W/nf + 0.29)' nrd='0.29 / W' nrs='0.29 / W'
+ sa=0 sb=0 sd=0 mult=1 m=1
XM86 net35 Vb net36 GND sky130_fd_pr__nfet_01v8 L=0.5 W=6 nf=1 ad='int((nf+1)/2) * W/nf * 0.29' as='int((nf+2)/2) * W/nf * 0.29'
+ pd='2*int((nf+1)/2) * (W/nf + 0.29)' ps='2*int((nf+2)/2) * (W/nf + 0.29)' nrd='0.29 / W' nrs='0.29 / W'
+ sa=0 sb=0 sd=0 mult=1 m=1
XM87 net36 Vb net35 GND sky130_fd_pr__nfet_01v8 L=0.5 W=6 nf=1 ad='int((nf+1)/2) * W/nf * 0.29' as='int((nf+2)/2) * W/nf * 0.29'
+ pd='2*int((nf+1)/2) * (W/nf + 0.29)' ps='2*int((nf+2)/2) * (W/nf + 0.29)' nrd='0.29 / W' nrs='0.29 / W'
+ sa=0 sb=0 sd=0 mult=1 m=1
XM88 net35 Vb net36 GND sky130_fd_pr__nfet_01v8 L=0.5 W=6 nf=1 ad='int((nf+1)/2) * W/nf * 0.29' as='int((nf+2)/2) * W/nf * 0.29'
+ pd='2*int((nf+1)/2) * (W/nf + 0.29)' ps='2*int((nf+2)/2) * (W/nf + 0.29)' nrd='0.29 / W' nrs='0.29 / W'
+ sa=0 sb=0 sd=0 mult=1 m=1
XM89 net36 Vb net35 GND sky130_fd_pr__nfet_01v8 L=0.5 W=6 nf=1 ad='int((nf+1)/2) * W/nf * 0.29' as='int((nf+2)/2) * W/nf * 0.29'
+ pd='2*int((nf+1)/2) * (W/nf + 0.29)' ps='2*int((nf+2)/2) * (W/nf + 0.29)' nrd='0.29 / W' nrs='0.29 / W'
+ sa=0 sb=0 sd=0 mult=1 m=1
XM90 net35 Vb net36 GND sky130_fd_pr__nfet_01v8 L=0.5 W=6 nf=1 ad='int((nf+1)/2) * W/nf * 0.29' as='int((nf+2)/2) * W/nf * 0.29'
+ pd='2*int((nf+1)/2) * (W/nf + 0.29)' ps='2*int((nf+2)/2) * (W/nf + 0.29)' nrd='0.29 / W' nrs='0.29 / W'
+ sa=0 sb=0 sd=0 mult=1 m=1
XM91 net36 Vb net35 GND sky130_fd_pr__nfet_01v8 L=0.5 W=6 nf=1 ad='int((nf+1)/2) * W/nf * 0.29' as='int((nf+2)/2) * W/nf * 0.29'
+ pd='2*int((nf+1)/2) * (W/nf + 0.29)' ps='2*int((nf+2)/2) * (W/nf + 0.29)' nrd='0.29 / W' nrs='0.29 / W'
+ sa=0 sb=0 sd=0 mult=1 m=1
XM92 net35 Vb net36 GND sky130_fd_pr__nfet_01v8 L=0.5 W=6 nf=1 ad='int((nf+1)/2) * W/nf * 0.29' as='int((nf+2)/2) * W/nf * 0.29'
+ pd='2*int((nf+1)/2) * (W/nf + 0.29)' ps='2*int((nf+2)/2) * (W/nf + 0.29)' nrd='0.29 / W' nrs='0.29 / W'
+ sa=0 sb=0 sd=0 mult=1 m=1
XM93 net36 Vb net35 GND sky130_fd_pr__nfet_01v8 L=0.5 W=6 nf=1 ad='int((nf+1)/2) * W/nf * 0.29' as='int((nf+2)/2) * W/nf * 0.29'
+ pd='2*int((nf+1)/2) * (W/nf + 0.29)' ps='2*int((nf+2)/2) * (W/nf + 0.29)' nrd='0.29 / W' nrs='0.29 / W'
+ sa=0 sb=0 sd=0 mult=1 m=1
XM94 net35 Vb net36 GND sky130_fd_pr__nfet_01v8 L=0.5 W=6 nf=1 ad='int((nf+1)/2) * W/nf * 0.29' as='int((nf+2)/2) * W/nf * 0.29'
+ pd='2*int((nf+1)/2) * (W/nf + 0.29)' ps='2*int((nf+2)/2) * (W/nf + 0.29)' nrd='0.29 / W' nrs='0.29 / W'
+ sa=0 sb=0 sd=0 mult=1 m=1
XM95 net36 Vb net35 GND sky130_fd_pr__nfet_01v8 L=0.5 W=6 nf=1 ad='int((nf+1)/2) * W/nf * 0.29' as='int((nf+2)/2) * W/nf * 0.29'
+ pd='2*int((nf+1)/2) * (W/nf + 0.29)' ps='2*int((nf+2)/2) * (W/nf + 0.29)' nrd='0.29 / W' nrs='0.29 / W'
+ sa=0 sb=0 sd=0 mult=1 m=1
XM96 net35 Vb net36 GND sky130_fd_pr__nfet_01v8 L=0.5 W=6 nf=1 ad='int((nf+1)/2) * W/nf * 0.29' as='int((nf+2)/2) * W/nf * 0.29'
+ pd='2*int((nf+1)/2) * (W/nf + 0.29)' ps='2*int((nf+2)/2) * (W/nf + 0.29)' nrd='0.29 / W' nrs='0.29 / W'
+ sa=0 sb=0 sd=0 mult=1 m=1
XM97 net36 Vb net35 GND sky130_fd_pr__nfet_01v8 L=0.5 W=6 nf=1 ad='int((nf+1)/2) * W/nf * 0.29' as='int((nf+2)/2) * W/nf * 0.29'
+ pd='2*int((nf+1)/2) * (W/nf + 0.29)' ps='2*int((nf+2)/2) * (W/nf + 0.29)' nrd='0.29 / W' nrs='0.29 / W'
+ sa=0 sb=0 sd=0 mult=1 m=1
XM98 net35 Vb net36 GND sky130_fd_pr__nfet_01v8 L=0.5 W=6 nf=1 ad='int((nf+1)/2) * W/nf * 0.29' as='int((nf+2)/2) * W/nf * 0.29'
+ pd='2*int((nf+1)/2) * (W/nf + 0.29)' ps='2*int((nf+2)/2) * (W/nf + 0.29)' nrd='0.29 / W' nrs='0.29 / W'
+ sa=0 sb=0 sd=0 mult=1 m=1
XM99 net36 Vb net35 GND sky130_fd_pr__nfet_01v8 L=0.5 W=6 nf=1 ad='int((nf+1)/2) * W/nf * 0.29' as='int((nf+2)/2) * W/nf * 0.29'
+ pd='2*int((nf+1)/2) * (W/nf + 0.29)' ps='2*int((nf+2)/2) * (W/nf + 0.29)' nrd='0.29 / W' nrs='0.29 / W'
+ sa=0 sb=0 sd=0 mult=1 m=1
XM100 net35 Vb net36 GND sky130_fd_pr__nfet_01v8 L=0.5 W=6 nf=1 ad='int((nf+1)/2) * W/nf * 0.29' as='int((nf+2)/2) * W/nf * 0.29'
+ pd='2*int((nf+1)/2) * (W/nf + 0.29)' ps='2*int((nf+2)/2) * (W/nf + 0.29)' nrd='0.29 / W' nrs='0.29 / W'
+ sa=0 sb=0 sd=0 mult=1 m=1
XM101 net36 Vb net35 GND sky130_fd_pr__nfet_01v8 L=0.5 W=6 nf=1 ad='int((nf+1)/2) * W/nf * 0.29' as='int((nf+2)/2) * W/nf * 0.29'
+ pd='2*int((nf+1)/2) * (W/nf + 0.29)' ps='2*int((nf+2)/2) * (W/nf + 0.29)' nrd='0.29 / W' nrs='0.29 / W'
+ sa=0 sb=0 sd=0 mult=1 m=1
XM102 Vb Vb GND GND sky130_fd_pr__nfet_01v8 L=0.5 W=6 nf=1 ad='int((nf+1)/2) * W/nf * 0.29' as='int((nf+2)/2) * W/nf * 0.29'
+ pd='2*int((nf+1)/2) * (W/nf + 0.29)' ps='2*int((nf+2)/2) * (W/nf + 0.29)' nrd='0.29 / W' nrs='0.29 / W'
+ sa=0 sb=0 sd=0 mult=1 m=1
XM103 VDD net36 Vb VDD sky130_fd_pr__pfet_01v8 L=0.5 W=6 nf=1 ad='int((nf+1)/2) * W/nf * 0.29' as='int((nf+2)/2) * W/nf * 0.29'
+ pd='2*int((nf+1)/2) * (W/nf + 0.29)' ps='2*int((nf+2)/2) * (W/nf + 0.29)' nrd='0.29 / W' nrs='0.29 / W'
+ sa=0 sb=0 sd=0 mult=1 m=1
XM104 net36 net36 VDD VDD sky130_fd_pr__pfet_01v8 L=0.5 W=6 nf=1 ad='int((nf+1)/2) * W/nf * 0.29' as='int((nf+2)/2) * W/nf * 0.29'
+ pd='2*int((nf+1)/2) * (W/nf + 0.29)' ps='2*int((nf+2)/2) * (W/nf + 0.29)' nrd='0.29 / W' nrs='0.29 / W'
+ sa=0 sb=0 sd=0 mult=1 m=1
XM105 VDD net36 net36 VDD sky130_fd_pr__pfet_01v8 L=0.5 W=6 nf=1 ad='int((nf+1)/2) * W/nf * 0.29' as='int((nf+2)/2) * W/nf * 0.29'
+ pd='2*int((nf+1)/2) * (W/nf + 0.29)' ps='2*int((nf+2)/2) * (W/nf + 0.29)' nrd='0.29 / W' nrs='0.29 / W'
+ sa=0 sb=0 sd=0 mult=1 m=1
XM106 Vb net36 VDD VDD sky130_fd_pr__pfet_01v8 L=0.5 W=6 nf=1 ad='int((nf+1)/2) * W/nf * 0.29' as='int((nf+2)/2) * W/nf * 0.29'
+ pd='2*int((nf+1)/2) * (W/nf + 0.29)' ps='2*int((nf+2)/2) * (W/nf + 0.29)' nrd='0.29 / W' nrs='0.29 / W'
+ sa=0 sb=0 sd=0 mult=1 m=1
R3 net35 GND 2.2k m=1
XM107 GND Vcp Vcp GND sky130_fd_pr__nfet_01v8 L=0.5 W=6 nf=1 ad='int((nf+1)/2) * W/nf * 0.29' as='int((nf+2)/2) * W/nf * 0.29'
+ pd='2*int((nf+1)/2) * (W/nf + 0.29)' ps='2*int((nf+2)/2) * (W/nf + 0.29)' nrd='0.29 / W' nrs='0.29 / W'
+ sa=0 sb=0 sd=0 mult=1 m=1
XM108 net37 Vcp net38 GND sky130_fd_pr__nfet_01v8 L=0.5 W=6 nf=1 ad='int((nf+1)/2) * W/nf * 0.29' as='int((nf+2)/2) * W/nf * 0.29'
+ pd='2*int((nf+1)/2) * (W/nf + 0.29)' ps='2*int((nf+2)/2) * (W/nf + 0.29)' nrd='0.29 / W' nrs='0.29 / W'
+ sa=0 sb=0 sd=0 mult=1 m=1
XM109 net38 Vcp net37 GND sky130_fd_pr__nfet_01v8 L=0.5 W=6 nf=1 ad='int((nf+1)/2) * W/nf * 0.29' as='int((nf+2)/2) * W/nf * 0.29'
+ pd='2*int((nf+1)/2) * (W/nf + 0.29)' ps='2*int((nf+2)/2) * (W/nf + 0.29)' nrd='0.29 / W' nrs='0.29 / W'
+ sa=0 sb=0 sd=0 mult=1 m=1
XM110 net37 Vcp net38 GND sky130_fd_pr__nfet_01v8 L=0.5 W=6 nf=1 ad='int((nf+1)/2) * W/nf * 0.29' as='int((nf+2)/2) * W/nf * 0.29'
+ pd='2*int((nf+1)/2) * (W/nf + 0.29)' ps='2*int((nf+2)/2) * (W/nf + 0.29)' nrd='0.29 / W' nrs='0.29 / W'
+ sa=0 sb=0 sd=0 mult=1 m=1
XM111 net38 Vcp net37 GND sky130_fd_pr__nfet_01v8 L=0.5 W=6 nf=1 ad='int((nf+1)/2) * W/nf * 0.29' as='int((nf+2)/2) * W/nf * 0.29'
+ pd='2*int((nf+1)/2) * (W/nf + 0.29)' ps='2*int((nf+2)/2) * (W/nf + 0.29)' nrd='0.29 / W' nrs='0.29 / W'
+ sa=0 sb=0 sd=0 mult=1 m=1
XM112 net37 Vcp net38 GND sky130_fd_pr__nfet_01v8 L=0.5 W=6 nf=1 ad='int((nf+1)/2) * W/nf * 0.29' as='int((nf+2)/2) * W/nf * 0.29'
+ pd='2*int((nf+1)/2) * (W/nf + 0.29)' ps='2*int((nf+2)/2) * (W/nf + 0.29)' nrd='0.29 / W' nrs='0.29 / W'
+ sa=0 sb=0 sd=0 mult=1 m=1
XM113 net38 Vcp net37 GND sky130_fd_pr__nfet_01v8 L=0.5 W=6 nf=1 ad='int((nf+1)/2) * W/nf * 0.29' as='int((nf+2)/2) * W/nf * 0.29'
+ pd='2*int((nf+1)/2) * (W/nf + 0.29)' ps='2*int((nf+2)/2) * (W/nf + 0.29)' nrd='0.29 / W' nrs='0.29 / W'
+ sa=0 sb=0 sd=0 mult=1 m=1
XM114 net37 Vcp net38 GND sky130_fd_pr__nfet_01v8 L=0.5 W=6 nf=1 ad='int((nf+1)/2) * W/nf * 0.29' as='int((nf+2)/2) * W/nf * 0.29'
+ pd='2*int((nf+1)/2) * (W/nf + 0.29)' ps='2*int((nf+2)/2) * (W/nf + 0.29)' nrd='0.29 / W' nrs='0.29 / W'
+ sa=0 sb=0 sd=0 mult=1 m=1
XM115 net38 Vcp net37 GND sky130_fd_pr__nfet_01v8 L=0.5 W=6 nf=1 ad='int((nf+1)/2) * W/nf * 0.29' as='int((nf+2)/2) * W/nf * 0.29'
+ pd='2*int((nf+1)/2) * (W/nf + 0.29)' ps='2*int((nf+2)/2) * (W/nf + 0.29)' nrd='0.29 / W' nrs='0.29 / W'
+ sa=0 sb=0 sd=0 mult=1 m=1
XM116 net37 Vcp net38 GND sky130_fd_pr__nfet_01v8 L=0.5 W=6 nf=1 ad='int((nf+1)/2) * W/nf * 0.29' as='int((nf+2)/2) * W/nf * 0.29'
+ pd='2*int((nf+1)/2) * (W/nf + 0.29)' ps='2*int((nf+2)/2) * (W/nf + 0.29)' nrd='0.29 / W' nrs='0.29 / W'
+ sa=0 sb=0 sd=0 mult=1 m=1
XM117 net38 Vcp net37 GND sky130_fd_pr__nfet_01v8 L=0.5 W=6 nf=1 ad='int((nf+1)/2) * W/nf * 0.29' as='int((nf+2)/2) * W/nf * 0.29'
+ pd='2*int((nf+1)/2) * (W/nf + 0.29)' ps='2*int((nf+2)/2) * (W/nf + 0.29)' nrd='0.29 / W' nrs='0.29 / W'
+ sa=0 sb=0 sd=0 mult=1 m=1
XM118 net37 Vcp net38 GND sky130_fd_pr__nfet_01v8 L=0.5 W=6 nf=1 ad='int((nf+1)/2) * W/nf * 0.29' as='int((nf+2)/2) * W/nf * 0.29'
+ pd='2*int((nf+1)/2) * (W/nf + 0.29)' ps='2*int((nf+2)/2) * (W/nf + 0.29)' nrd='0.29 / W' nrs='0.29 / W'
+ sa=0 sb=0 sd=0 mult=1 m=1
XM119 net38 Vcp net37 GND sky130_fd_pr__nfet_01v8 L=0.5 W=6 nf=1 ad='int((nf+1)/2) * W/nf * 0.29' as='int((nf+2)/2) * W/nf * 0.29'
+ pd='2*int((nf+1)/2) * (W/nf + 0.29)' ps='2*int((nf+2)/2) * (W/nf + 0.29)' nrd='0.29 / W' nrs='0.29 / W'
+ sa=0 sb=0 sd=0 mult=1 m=1
XM120 net37 Vcp net38 GND sky130_fd_pr__nfet_01v8 L=0.5 W=6 nf=1 ad='int((nf+1)/2) * W/nf * 0.29' as='int((nf+2)/2) * W/nf * 0.29'
+ pd='2*int((nf+1)/2) * (W/nf + 0.29)' ps='2*int((nf+2)/2) * (W/nf + 0.29)' nrd='0.29 / W' nrs='0.29 / W'
+ sa=0 sb=0 sd=0 mult=1 m=1
XM121 net38 Vcp net37 GND sky130_fd_pr__nfet_01v8 L=0.5 W=6 nf=1 ad='int((nf+1)/2) * W/nf * 0.29' as='int((nf+2)/2) * W/nf * 0.29'
+ pd='2*int((nf+1)/2) * (W/nf + 0.29)' ps='2*int((nf+2)/2) * (W/nf + 0.29)' nrd='0.29 / W' nrs='0.29 / W'
+ sa=0 sb=0 sd=0 mult=1 m=1
XM122 net37 Vcp net38 GND sky130_fd_pr__nfet_01v8 L=0.5 W=6 nf=1 ad='int((nf+1)/2) * W/nf * 0.29' as='int((nf+2)/2) * W/nf * 0.29'
+ pd='2*int((nf+1)/2) * (W/nf + 0.29)' ps='2*int((nf+2)/2) * (W/nf + 0.29)' nrd='0.29 / W' nrs='0.29 / W'
+ sa=0 sb=0 sd=0 mult=1 m=1
XM123 net38 Vcp net37 GND sky130_fd_pr__nfet_01v8 L=0.5 W=6 nf=1 ad='int((nf+1)/2) * W/nf * 0.29' as='int((nf+2)/2) * W/nf * 0.29'
+ pd='2*int((nf+1)/2) * (W/nf + 0.29)' ps='2*int((nf+2)/2) * (W/nf + 0.29)' nrd='0.29 / W' nrs='0.29 / W'
+ sa=0 sb=0 sd=0 mult=1 m=1
XM124 Vcp Vcp GND GND sky130_fd_pr__nfet_01v8 L=0.5 W=6 nf=1 ad='int((nf+1)/2) * W/nf * 0.29' as='int((nf+2)/2) * W/nf * 0.29'
+ pd='2*int((nf+1)/2) * (W/nf + 0.29)' ps='2*int((nf+2)/2) * (W/nf + 0.29)' nrd='0.29 / W' nrs='0.29 / W'
+ sa=0 sb=0 sd=0 mult=1 m=1
XM125 VDD net38 Vcp VDD sky130_fd_pr__pfet_01v8 L=0.5 W=6 nf=1 ad='int((nf+1)/2) * W/nf * 0.29' as='int((nf+2)/2) * W/nf * 0.29'
+ pd='2*int((nf+1)/2) * (W/nf + 0.29)' ps='2*int((nf+2)/2) * (W/nf + 0.29)' nrd='0.29 / W' nrs='0.29 / W'
+ sa=0 sb=0 sd=0 mult=1 m=1
XM126 net38 net38 VDD VDD sky130_fd_pr__pfet_01v8 L=0.5 W=6 nf=1 ad='int((nf+1)/2) * W/nf * 0.29' as='int((nf+2)/2) * W/nf * 0.29'
+ pd='2*int((nf+1)/2) * (W/nf + 0.29)' ps='2*int((nf+2)/2) * (W/nf + 0.29)' nrd='0.29 / W' nrs='0.29 / W'
+ sa=0 sb=0 sd=0 mult=1 m=1
XM127 VDD net38 net38 VDD sky130_fd_pr__pfet_01v8 L=0.5 W=6 nf=1 ad='int((nf+1)/2) * W/nf * 0.29' as='int((nf+2)/2) * W/nf * 0.29'
+ pd='2*int((nf+1)/2) * (W/nf + 0.29)' ps='2*int((nf+2)/2) * (W/nf + 0.29)' nrd='0.29 / W' nrs='0.29 / W'
+ sa=0 sb=0 sd=0 mult=1 m=1
XM128 Vcp net38 VDD VDD sky130_fd_pr__pfet_01v8 L=0.5 W=6 nf=1 ad='int((nf+1)/2) * W/nf * 0.29' as='int((nf+2)/2) * W/nf * 0.29'
+ pd='2*int((nf+1)/2) * (W/nf + 0.29)' ps='2*int((nf+2)/2) * (W/nf + 0.29)' nrd='0.29 / W' nrs='0.29 / W'
+ sa=0 sb=0 sd=0 mult=1 m=1
R4 net37 GND 800 m=1
XM129 net41 net39 VDD VDD sky130_fd_pr__pfet_01v8 L={L} W={W} nf=1 ad='int((nf+1)/2) * W/nf * 0.29' as='int((nf+2)/2) * W/nf * 0.29'
+ pd='2*int((nf+1)/2) * (W/nf + 0.29)' ps='2*int((nf+2)/2) * (W/nf + 0.29)' nrd='0.29 / W' nrs='0.29 / W'
+ sa=0 sb=0 sd=0 mult=1 m=1
XM130 net39 net39 VDD VDD sky130_fd_pr__pfet_01v8 L={L} W={W} nf=1 ad='int((nf+1)/2) * W/nf * 0.29' as='int((nf+2)/2) * W/nf * 0.29'
+ pd='2*int((nf+1)/2) * (W/nf + 0.29)' ps='2*int((nf+2)/2) * (W/nf + 0.29)' nrd='0.29 / W' nrs='0.29 / W'
+ sa=0 sb=0 sd=0 mult=1 m=1
XM131 net40 net40 VDD VDD sky130_fd_pr__pfet_01v8 L={L} W={W} nf=1 ad='int((nf+1)/2) * W/nf * 0.29' as='int((nf+2)/2) * W/nf * 0.29'
+ pd='2*int((nf+1)/2) * (W/nf + 0.29)' ps='2*int((nf+2)/2) * (W/nf + 0.29)' nrd='0.29 / W' nrs='0.29 / W'
+ sa=0 sb=0 sd=0 mult=1 m=1
XM132 net42 net40 VDD VDD sky130_fd_pr__pfet_01v8 L={L} W={W} nf=1 ad='int((nf+1)/2) * W/nf * 0.29' as='int((nf+2)/2) * W/nf * 0.29'
+ pd='2*int((nf+1)/2) * (W/nf + 0.29)' ps='2*int((nf+2)/2) * (W/nf + 0.29)' nrd='0.29 / W' nrs='0.29 / W'
+ sa=0 sb=0 sd=0 mult=1 m=1
XM133 net44 Vcp net41 VDD sky130_fd_pr__pfet_01v8 L={L} W={W} nf=1 ad='int((nf+1)/2) * W/nf * 0.29' as='int((nf+2)/2) * W/nf * 0.29'
+ pd='2*int((nf+1)/2) * (W/nf + 0.29)' ps='2*int((nf+2)/2) * (W/nf + 0.29)' nrd='0.29 / W' nrs='0.29 / W'
+ sa=0 sb=0 sd=0 mult=1 m=1
XM134 CompOut Vcp net42 VDD sky130_fd_pr__pfet_01v8 L={L} W={W} nf=1 ad='int((nf+1)/2) * W/nf * 0.29'
+ as='int((nf+2)/2) * W/nf * 0.29' pd='2*int((nf+1)/2) * (W/nf + 0.29)' ps='2*int((nf+2)/2) * (W/nf + 0.29)'
+ nrd='0.29 / W' nrs='0.29 / W' sa=0 sb=0 sd=0 mult=1 m=1
XM135 net39 Vb GND GND sky130_fd_pr__nfet_01v8 L={L} W={W} nf=1 ad='int((nf+1)/2) * W/nf * 0.29' as='int((nf+2)/2) * W/nf * 0.29'
+ pd='2*int((nf+1)/2) * (W/nf + 0.29)' ps='2*int((nf+2)/2) * (W/nf + 0.29)' nrd='0.29 / W' nrs='0.29 / W'
+ sa=0 sb=0 sd=0 mult=1 m=1
XM136 net40 Vb GND GND sky130_fd_pr__nfet_01v8 L={L} W={W} nf=1 ad='int((nf+1)/2) * W/nf * 0.29' as='int((nf+2)/2) * W/nf * 0.29'
+ pd='2*int((nf+1)/2) * (W/nf + 0.29)' ps='2*int((nf+2)/2) * (W/nf + 0.29)' nrd='0.29 / W' nrs='0.29 / W'
+ sa=0 sb=0 sd=0 mult=1 m=1
XM137 net43 AIn net40 GND sky130_fd_pr__nfet_01v8 L={L} W={W} nf=1 ad='int((nf+1)/2) * W/nf * 0.29' as='int((nf+2)/2) * W/nf * 0.29'
+ pd='2*int((nf+1)/2) * (W/nf + 0.29)' ps='2*int((nf+2)/2) * (W/nf + 0.29)' nrd='0.29 / W' nrs='0.29 / W'
+ sa=0 sb=0 sd=0 mult=1 m=1
XM138 net39 C+ net43 GND sky130_fd_pr__nfet_01v8 L={L} W={W} nf=1 ad='int((nf+1)/2) * W/nf * 0.29' as='int((nf+2)/2) * W/nf * 0.29'
+ pd='2*int((nf+1)/2) * (W/nf + 0.29)' ps='2*int((nf+2)/2) * (W/nf + 0.29)' nrd='0.29 / W' nrs='0.29 / W'
+ sa=0 sb=0 sd=0 mult=1 m=1
XM139 net46 RST net45 GND sky130_fd_pr__nfet_01v8 L={L} W={W} nf=1 ad='int((nf+1)/2) * W/nf * 0.29' as='int((nf+2)/2) * W/nf * 0.29'
+ pd='2*int((nf+1)/2) * (W/nf + 0.29)' ps='2*int((nf+2)/2) * (W/nf + 0.29)' nrd='0.29 / W' nrs='0.29 / W'
+ sa=0 sb=0 sd=0 mult=1 m=1
C9 net45 GND 0.1p m=1
C10 net46 GND 0.1p m=1
XM140 GND Vb net43 GND sky130_fd_pr__nfet_01v8 L={L} W={W} nf=1 ad='int((nf+1)/2) * W/nf * 0.29' as='int((nf+2)/2) * W/nf * 0.29'
+ pd='2*int((nf+1)/2) * (W/nf + 0.29)' ps='2*int((nf+2)/2) * (W/nf + 0.29)' nrd='0.29 / W' nrs='0.29 / W'
+ sa=0 sb=0 sd=0 mult=1 m=1
XM141 CompOutb ENADb VDD VDD sky130_fd_pr__pfet_01v8 L={L} W={W} nf=1 ad='int((nf+1)/2) * W/nf * 0.29'
+ as='int((nf+2)/2) * W/nf * 0.29' pd='2*int((nf+1)/2) * (W/nf + 0.29)' ps='2*int((nf+2)/2) * (W/nf + 0.29)'
+ nrd='0.29 / W' nrs='0.29 / W' sa=0 sb=0 sd=0 mult=1 m=1
XM142 net45 ENADb net46 GND sky130_fd_pr__nfet_01v8 L={L} W={W} nf=1 ad='int((nf+1)/2) * W/nf * 0.29'
+ as='int((nf+2)/2) * W/nf * 0.29' pd='2*int((nf+1)/2) * (W/nf + 0.29)' ps='2*int((nf+2)/2) * (W/nf + 0.29)'
+ nrd='0.29 / W' nrs='0.29 / W' sa=0 sb=0 sd=0 mult=1 m=1
XM143 net47 ENAD net46 GND sky130_fd_pr__nfet_01v8 L={L} W={W} nf=1 ad='int((nf+1)/2) * W/nf * 0.29'
+ as='int((nf+2)/2) * W/nf * 0.29' pd='2*int((nf+1)/2) * (W/nf + 0.29)' ps='2*int((nf+2)/2) * (W/nf + 0.29)'
+ nrd='0.29 / W' nrs='0.29 / W' sa=0 sb=0 sd=0 mult=1 m=1
XM144 GND net48 net47 GND sky130_fd_pr__nfet_01v8 L={L} W={W} nf=1 ad='int((nf+1)/2) * W/nf * 0.29' as='int((nf+2)/2) * W/nf * 0.29'
+ pd='2*int((nf+1)/2) * (W/nf + 0.29)' ps='2*int((nf+2)/2) * (W/nf + 0.29)' nrd='0.29 / W' nrs='0.29 / W'
+ sa=0 sb=0 sd=0 mult=1 m=1
XM145 net47 CompOutb net44 GND sky130_fd_pr__nfet_01v8 L={L} W={W} nf=1 ad='int((nf+1)/2) * W/nf * 0.29'
+ as='int((nf+2)/2) * W/nf * 0.29' pd='2*int((nf+1)/2) * (W/nf + 0.29)' ps='2*int((nf+2)/2) * (W/nf + 0.29)'
+ nrd='0.29 / W' nrs='0.29 / W' sa=0 sb=0 sd=0 mult=1 m=1
XM146 CompOutb ENADb CompOut GND sky130_fd_pr__nfet_01v8 L={L} W={W} nf=1 ad='int((nf+1)/2) * W/nf * 0.29'
+ as='int((nf+2)/2) * W/nf * 0.29' pd='2*int((nf+1)/2) * (W/nf + 0.29)' ps='2*int((nf+2)/2) * (W/nf + 0.29)'
+ nrd='0.29 / W' nrs='0.29 / W' sa=0 sb=0 sd=0 mult=1 m=1
XM147 net48 net46 GND GND sky130_fd_pr__nfet_01v8 L={L} W={W} nf=1 ad='int((nf+1)/2) * W/nf * 0.29' as='int((nf+2)/2) * W/nf * 0.29'
+ pd='2*int((nf+1)/2) * (W/nf + 0.29)' ps='2*int((nf+2)/2) * (W/nf + 0.29)' nrd='0.29 / W' nrs='0.29 / W'
+ sa=0 sb=0 sd=0 mult=1 m=1
XM148 CompOut CompOutb net48 GND sky130_fd_pr__nfet_01v8 L={L} W={W} nf=1 ad='int((nf+1)/2) * W/nf * 0.29'
+ as='int((nf+2)/2) * W/nf * 0.29' pd='2*int((nf+1)/2) * (W/nf + 0.29)' ps='2*int((nf+2)/2) * (W/nf + 0.29)'
+ nrd='0.29 / W' nrs='0.29 / W' sa=0 sb=0 sd=0 mult=1 m=1
XM149 C+ SHb C- VDD sky130_fd_pr__pfet_01v8 L={L} W={W} nf=1 ad='int((nf+1)/2) * W/nf * 0.29' as='int((nf+2)/2) * W/nf * 0.29'
+ pd='2*int((nf+1)/2) * (W/nf + 0.29)' ps='2*int((nf+2)/2) * (W/nf + 0.29)' nrd='0.29 / W' nrs='0.29 / W'
+ sa=0 sb=0 sd=0 mult=1 m=1
XM150 C+ SH C- GND sky130_fd_pr__nfet_01v8 L={L} W={W} nf=1 ad='int((nf+1)/2) * W/nf * 0.29' as='int((nf+2)/2) * W/nf * 0.29'
+ pd='2*int((nf+1)/2) * (W/nf + 0.29)' ps='2*int((nf+2)/2) * (W/nf + 0.29)' nrd='0.29 / W' nrs='0.29 / W'
+ sa=0 sb=0 sd=0 mult=1 m=1
**.ends
.GLOBAL VDD
.GLOBAL GND
.end
